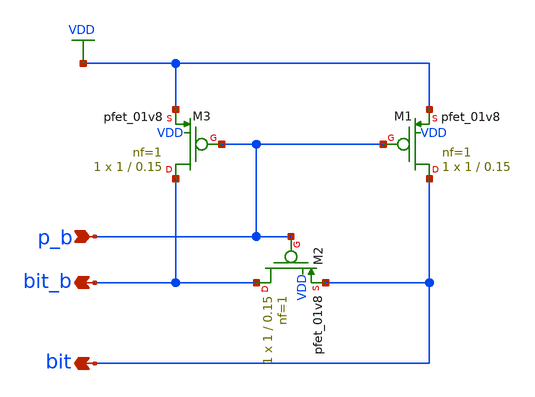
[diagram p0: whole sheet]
** sch_path: gates/Memory/precharge circuit.sch
**.subckt precharge circuit p_b bit_b bit
*.ipin p_b
*.opin bit_b
*.opin bit
XM1 bit p_b VDD VDD sky130_fd_pr__pfet_01v8 L=0.15 W=1 nf=1 ad='int((nf+1)/2) * W/nf * 0.29' as='int((nf+2)/2) * W/nf * 0.29'
+ pd='2*int((nf+1)/2) * (W/nf + 0.29)' ps='2*int((nf+2)/2) * (W/nf + 0.29)' nrd='0.29 / W' nrs='0.29 / W'
+ sa=0 sb=0 sd=0 mult=1 m=1
XM2 bit_b p_b bit VDD sky130_fd_pr__pfet_01v8 L=0.15 W=1 nf=1 ad='int((nf+1)/2) * W/nf * 0.29' as='int((nf+2)/2) * W/nf * 0.29'
+ pd='2*int((nf+1)/2) * (W/nf + 0.29)' ps='2*int((nf+2)/2) * (W/nf + 0.29)' nrd='0.29 / W' nrs='0.29 / W'
+ sa=0 sb=0 sd=0 mult=1 m=1
XM3 bit_b p_b VDD VDD sky130_fd_pr__pfet_01v8 L=0.15 W=1 nf=1 ad='int((nf+1)/2) * W/nf * 0.29' as='int((nf+2)/2) * W/nf * 0.29'
+ pd='2*int((nf+1)/2) * (W/nf + 0.29)' ps='2*int((nf+2)/2) * (W/nf + 0.29)' nrd='0.29 / W' nrs='0.29 / W'
+ sa=0 sb=0 sd=0 mult=1 m=1
**.ends
.GLOBAL VDD
.end
